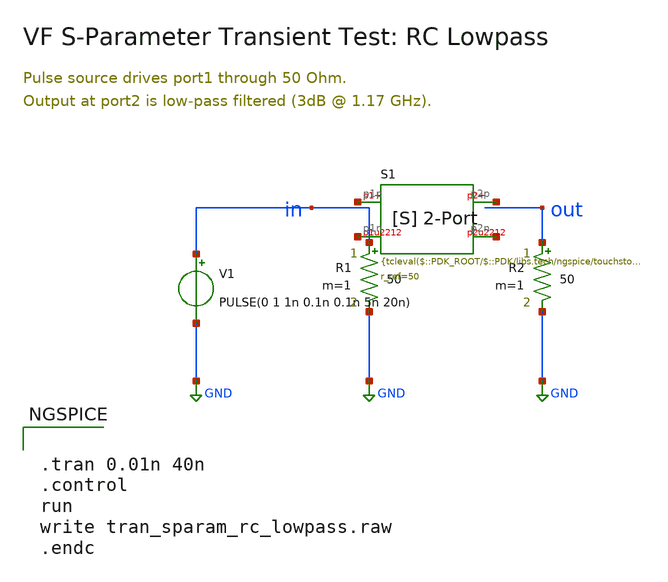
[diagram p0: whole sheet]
** sch_path: ihp-sg13g2/libs.tech/xschem/sg13g2_tests/tran_sparam_rc_lowpass.sch
* Copyright 2024 IHP PDK Authors
**.subckt tran_sparam_rc_lowpass
V1 in GND PULSE(0 1 1n 0.1n 0.1n 5n 20n)
R1 in GND 50 m=1
R2 out GND 50 m=1
AS1 [ net1 net2 net3 net4 ] lowpass_model
.model lowpass_model sparam( file=" r_ref=50 n_poles=0 vf_tol=1e-3 vf_maxiter=10 )
**** begin user architecture code


.tran 0.01n 40n
.control
run
write tran_sparam_rc_lowpass.raw
.endc


**** end user architecture code
**.ends
.GLOBAL GND
.end
